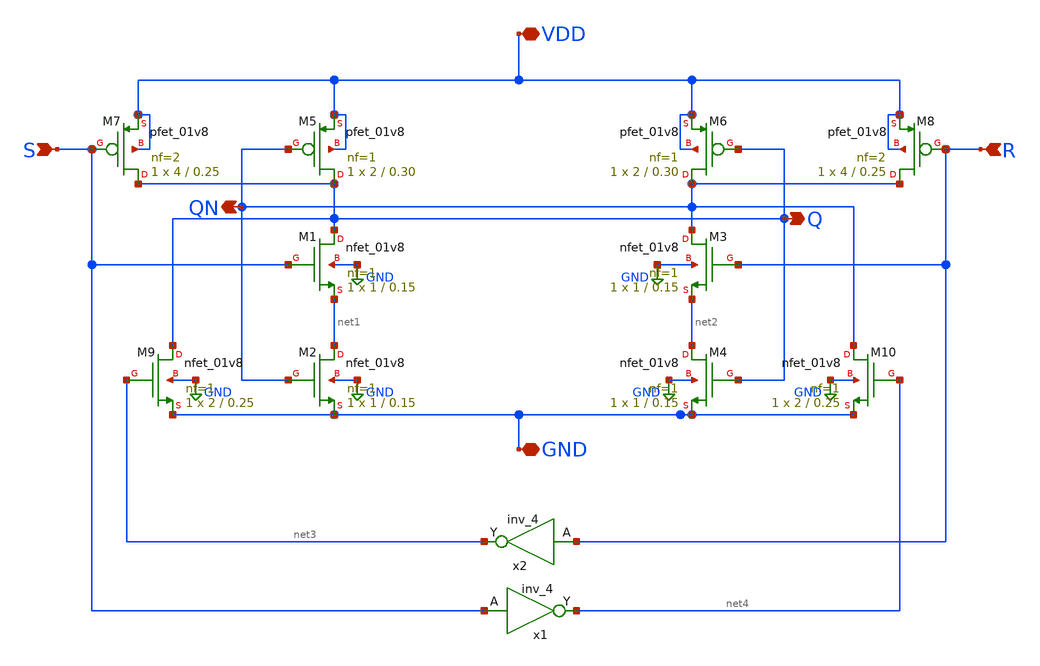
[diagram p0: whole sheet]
** sch_path: RSlatch/xschem/RSfetsym.sch
**.subckt RSfetsym Q QN S R VDD GND
*.opin Q
*.opin QN
*.ipin S
*.ipin R
*.iopin VDD
*.iopin GND
XM1 Q S net1 GND sky130_fd_pr__nfet_01v8 L=0.15 W=1 nf=1 ad='int((nf+1)/2) * W/nf * 0.29' as='int((nf+2)/2) * W/nf * 0.29'
+ pd='2*int((nf+1)/2) * (W/nf + 0.29)' ps='2*int((nf+2)/2) * (W/nf + 0.29)' nrd='0.29 / W' nrs='0.29 / W'
+ sa=0 sb=0 sd=0 mult=1 m=1
XM2 net1 QN GND GND sky130_fd_pr__nfet_01v8 L=0.15 W=1 nf=1 ad='int((nf+1)/2) * W/nf * 0.29' as='int((nf+2)/2) * W/nf * 0.29'
+ pd='2*int((nf+1)/2) * (W/nf + 0.29)' ps='2*int((nf+2)/2) * (W/nf + 0.29)' nrd='0.29 / W' nrs='0.29 / W'
+ sa=0 sb=0 sd=0 mult=1 m=1
XM3 QN R net2 GND sky130_fd_pr__nfet_01v8 L=0.15 W=1 nf=1 ad='int((nf+1)/2) * W/nf * 0.29' as='int((nf+2)/2) * W/nf * 0.29'
+ pd='2*int((nf+1)/2) * (W/nf + 0.29)' ps='2*int((nf+2)/2) * (W/nf + 0.29)' nrd='0.29 / W' nrs='0.29 / W'
+ sa=0 sb=0 sd=0 mult=1 m=1
XM4 net2 Q GND GND sky130_fd_pr__nfet_01v8 L=0.15 W=1 nf=1 ad='int((nf+1)/2) * W/nf * 0.29' as='int((nf+2)/2) * W/nf * 0.29'
+ pd='2*int((nf+1)/2) * (W/nf + 0.29)' ps='2*int((nf+2)/2) * (W/nf + 0.29)' nrd='0.29 / W' nrs='0.29 / W'
+ sa=0 sb=0 sd=0 mult=1 m=1
XM5 Q QN VDD VDD sky130_fd_pr__pfet_01v8 L=0.30 W=2 nf=1 ad='int((nf+1)/2) * W/nf * 0.29' as='int((nf+2)/2) * W/nf * 0.29'
+ pd='2*int((nf+1)/2) * (W/nf + 0.29)' ps='2*int((nf+2)/2) * (W/nf + 0.29)' nrd='0.29 / W' nrs='0.29 / W'
+ sa=0 sb=0 sd=0 mult=1 m=1
XM6 QN Q VDD VDD sky130_fd_pr__pfet_01v8 L=0.30 W=2 nf=1 ad='int((nf+1)/2) * W/nf * 0.29' as='int((nf+2)/2) * W/nf * 0.29'
+ pd='2*int((nf+1)/2) * (W/nf + 0.29)' ps='2*int((nf+2)/2) * (W/nf + 0.29)' nrd='0.29 / W' nrs='0.29 / W'
+ sa=0 sb=0 sd=0 mult=1 m=1
XM7 Q S VDD VDD sky130_fd_pr__pfet_01v8 L=0.25 W=4 nf=2 ad='int((nf+1)/2) * W/nf * 0.29' as='int((nf+2)/2) * W/nf * 0.29'
+ pd='2*int((nf+1)/2) * (W/nf + 0.29)' ps='2*int((nf+2)/2) * (W/nf + 0.29)' nrd='0.29 / W' nrs='0.29 / W'
+ sa=0 sb=0 sd=0 mult=1 m=1
XM8 QN R VDD VDD sky130_fd_pr__pfet_01v8 L=0.25 W=4 nf=2 ad='int((nf+1)/2) * W/nf * 0.29' as='int((nf+2)/2) * W/nf * 0.29'
+ pd='2*int((nf+1)/2) * (W/nf + 0.29)' ps='2*int((nf+2)/2) * (W/nf + 0.29)' nrd='0.29 / W' nrs='0.29 / W'
+ sa=0 sb=0 sd=0 mult=1 m=1
XM9 Q net3 GND GND sky130_fd_pr__nfet_01v8 L=0.25 W=2 nf=1 ad='int((nf+1)/2) * W/nf * 0.29' as='int((nf+2)/2) * W/nf * 0.29'
+ pd='2*int((nf+1)/2) * (W/nf + 0.29)' ps='2*int((nf+2)/2) * (W/nf + 0.29)' nrd='0.29 / W' nrs='0.29 / W'
+ sa=0 sb=0 sd=0 mult=1 m=1
XM10 QN net4 GND GND sky130_fd_pr__nfet_01v8 L=0.25 W=2 nf=1 ad='int((nf+1)/2) * W/nf * 0.29' as='int((nf+2)/2) * W/nf * 0.29'
+ pd='2*int((nf+1)/2) * (W/nf + 0.29)' ps='2*int((nf+2)/2) * (W/nf + 0.29)' nrd='0.29 / W' nrs='0.29 / W'
+ sa=0 sb=0 sd=0 mult=1 m=1
x2 R GND GND VDD VDD net3 sky130_fd_sc_hd__inv_4
x1 S GND GND VDD VDD net4 sky130_fd_sc_hd__inv_4
**.ends
.GLOBAL GND
.end
